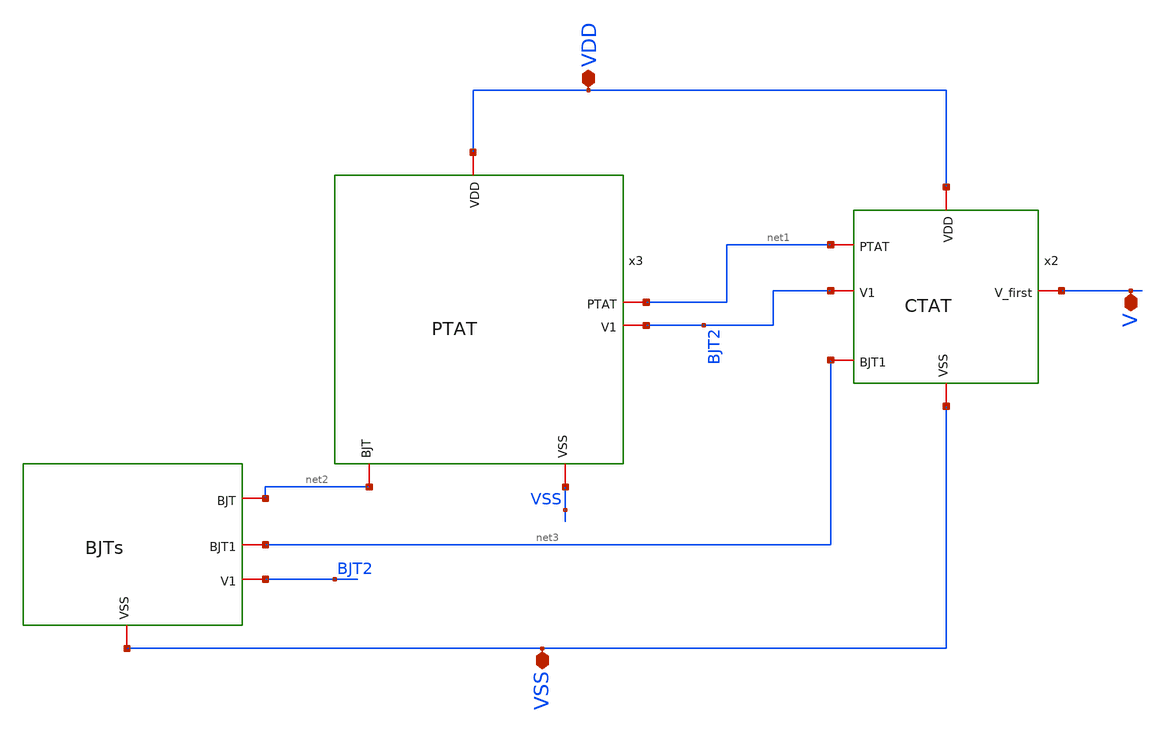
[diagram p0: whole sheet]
** sch_path: xschem/xschem_BGR_Top/1st_order_BGR_TOP.sch
**.subckt 1st_order_BGR_TOP VDD VSS V
*.iopin VDD
*.iopin VSS
*.iopin V
x1 net2 VSS net3 BJT2 BJTs
x2 VDD net1 BJT2 V VSS net3 CTAT
x3 VDD net1 BJT2 net2 VSS PTAT
**.ends

* expanding   symbol:  BJTs.sym # of pins=4
** sym_path: xschem/xschem_BGR_Top/BJTs.sym
** sch_path: xschem/xschem_BGR_Top/BJTs.sch
.subckt BJTs BJT VSS BJT1 V1
*.iopin VSS
*.iopin BJT
*.iopin BJT1
*.iopin V1
XQ10 VSS VSS BJT sky130_fd_pr__pnp_05v5_W3p40L3p40 m=1
XQ11 VSS VSS BJT sky130_fd_pr__pnp_05v5_W3p40L3p40 m=1
XQ13 VSS VSS BJT sky130_fd_pr__pnp_05v5_W3p40L3p40 m=1
XQ14 VSS VSS BJT sky130_fd_pr__pnp_05v5_W3p40L3p40 m=1
XQ15 VSS VSS BJT sky130_fd_pr__pnp_05v5_W3p40L3p40 m=1
XQ12 VSS VSS BJT1 sky130_fd_pr__pnp_05v5_W3p40L3p40 m=1
XQ9 VSS VSS V1 sky130_fd_pr__pnp_05v5_W3p40L3p40 m=1
.ends


* expanding   symbol:  CTAT.sym # of pins=6
** sym_path: xschem/xschem_BGR_Top/CTAT.sym
** sch_path: xschem/xschem_BGR_Top/CTAT.sch
.subckt CTAT VDD PTAT V1 V_first VSS BJT1
*.iopin VDD
*.iopin PTAT
*.iopin V1
*.iopin BJT1
*.iopin V_first
*.iopin VSS
XM27 net1 PTAT VDD VDD sky130_fd_pr__pfet_g5v0d10v5 L=5 W=15 nf=1 ad='int((nf+1)/2) * W/nf * 0.29' as='int((nf+2)/2) * W/nf * 0.29'
+ pd='2*int((nf+1)/2) * (W/nf + 0.29)' ps='2*int((nf+2)/2) * (W/nf + 0.29)' nrd='0.29 / W' nrs='0.29 / W'
+ sa=0 sb=0 sd=0 mult=1 m=1
XM28 V_first V1 net1 VDD sky130_fd_pr__pfet_g5v0d10v5 L=5 W=30 nf=2 ad='int((nf+1)/2) * W/nf * 0.29'
+ as='int((nf+2)/2) * W/nf * 0.29' pd='2*int((nf+1)/2) * (W/nf + 0.29)' ps='2*int((nf+2)/2) * (W/nf + 0.29)'
+ nrd='0.29 / W' nrs='0.29 / W' sa=0 sb=0 sd=0 mult=1 m=1
XR2 net2 V_first VSS sky130_fd_pr__res_high_po_0p35 L=44.43 mult=1 m=1
XR1 BJT1 net2 VSS sky130_fd_pr__res_high_po_0p35 L=44.43 mult=1 m=1
XR3 VSS VSS VSS sky130_fd_pr__res_high_po_0p35 L=44.43 mult=1 m=1
XR4 VSS VSS VSS sky130_fd_pr__res_high_po_0p35 L=44.43 mult=1 m=1
.ends


* expanding   symbol:  PTAT.sym # of pins=5
** sym_path: xschem/xschem_BGR_Top/PTAT.sym
** sch_path: xschem/xschem_BGR_Top/PTAT.sch
.subckt PTAT VDD PTAT V1 BJT VSS
*.iopin VDD
*.iopin PTAT
*.iopin V1
*.iopin BJT
*.iopin VSS
XM22 PTAT net3 net4 VSS sky130_fd_pr__nfet_g5v0d10v5 L=5 W=15 nf=1 ad='int((nf+1)/2) * W/nf * 0.29' as='int((nf+2)/2) * W/nf * 0.29'
+ pd='2*int((nf+1)/2) * (W/nf + 0.29)' ps='2*int((nf+2)/2) * (W/nf + 0.29)' nrd='0.29 / W' nrs='0.29 / W'
+ sa=0 sb=0 sd=0 mult=1 m=1
XM23 net3 net3 V1 VSS sky130_fd_pr__nfet_g5v0d10v5 L=5 W=15 nf=1 ad='int((nf+1)/2) * W/nf * 0.29' as='int((nf+2)/2) * W/nf * 0.29'
+ pd='2*int((nf+1)/2) * (W/nf + 0.29)' ps='2*int((nf+2)/2) * (W/nf + 0.29)' nrd='0.29 / W' nrs='0.29 / W'
+ sa=0 sb=0 sd=0 mult=1 m=1
XM24 net1 PTAT VDD VDD sky130_fd_pr__pfet_g5v0d10v5 L=5 W=15 nf=1 ad='int((nf+1)/2) * W/nf * 0.29' as='int((nf+2)/2) * W/nf * 0.29'
+ pd='2*int((nf+1)/2) * (W/nf + 0.29)' ps='2*int((nf+2)/2) * (W/nf + 0.29)' nrd='0.29 / W' nrs='0.29 / W'
+ sa=0 sb=0 sd=0 mult=1 m=1
XM25 net3 net4 net1 VDD sky130_fd_pr__pfet_g5v0d10v5 L=5 W=30 nf=2 ad='int((nf+1)/2) * W/nf * 0.29' as='int((nf+2)/2) * W/nf * 0.29'
+ pd='2*int((nf+1)/2) * (W/nf + 0.29)' ps='2*int((nf+2)/2) * (W/nf + 0.29)' nrd='0.29 / W' nrs='0.29 / W'
+ sa=0 sb=0 sd=0 mult=1 m=1
XM26 net2 PTAT VDD VDD sky130_fd_pr__pfet_g5v0d10v5 L=5 W=15 nf=1 ad='int((nf+1)/2) * W/nf * 0.29' as='int((nf+2)/2) * W/nf * 0.29'
+ pd='2*int((nf+1)/2) * (W/nf + 0.29)' ps='2*int((nf+2)/2) * (W/nf + 0.29)' nrd='0.29 / W' nrs='0.29 / W'
+ sa=0 sb=0 sd=0 mult=1 m=1
XM29 PTAT V1 net2 VDD sky130_fd_pr__pfet_g5v0d10v5 L=5 W=30 nf=2 ad='int((nf+1)/2) * W/nf * 0.29' as='int((nf+2)/2) * W/nf * 0.29'
+ pd='2*int((nf+1)/2) * (W/nf + 0.29)' ps='2*int((nf+2)/2) * (W/nf + 0.29)' nrd='0.29 / W' nrs='0.29 / W'
+ sa=0 sb=0 sd=0 mult=1 m=1
XR1 BJT net4 VSS sky130_fd_pr__res_high_po_0p35 L=8 mult=1 m=1
XR2 VSS VSS VSS sky130_fd_pr__res_high_po_0p35 L=8 mult=1 m=1
XR3 VSS VSS VSS sky130_fd_pr__res_high_po_0p35 L=8 mult=1 m=1
.ends

.end
